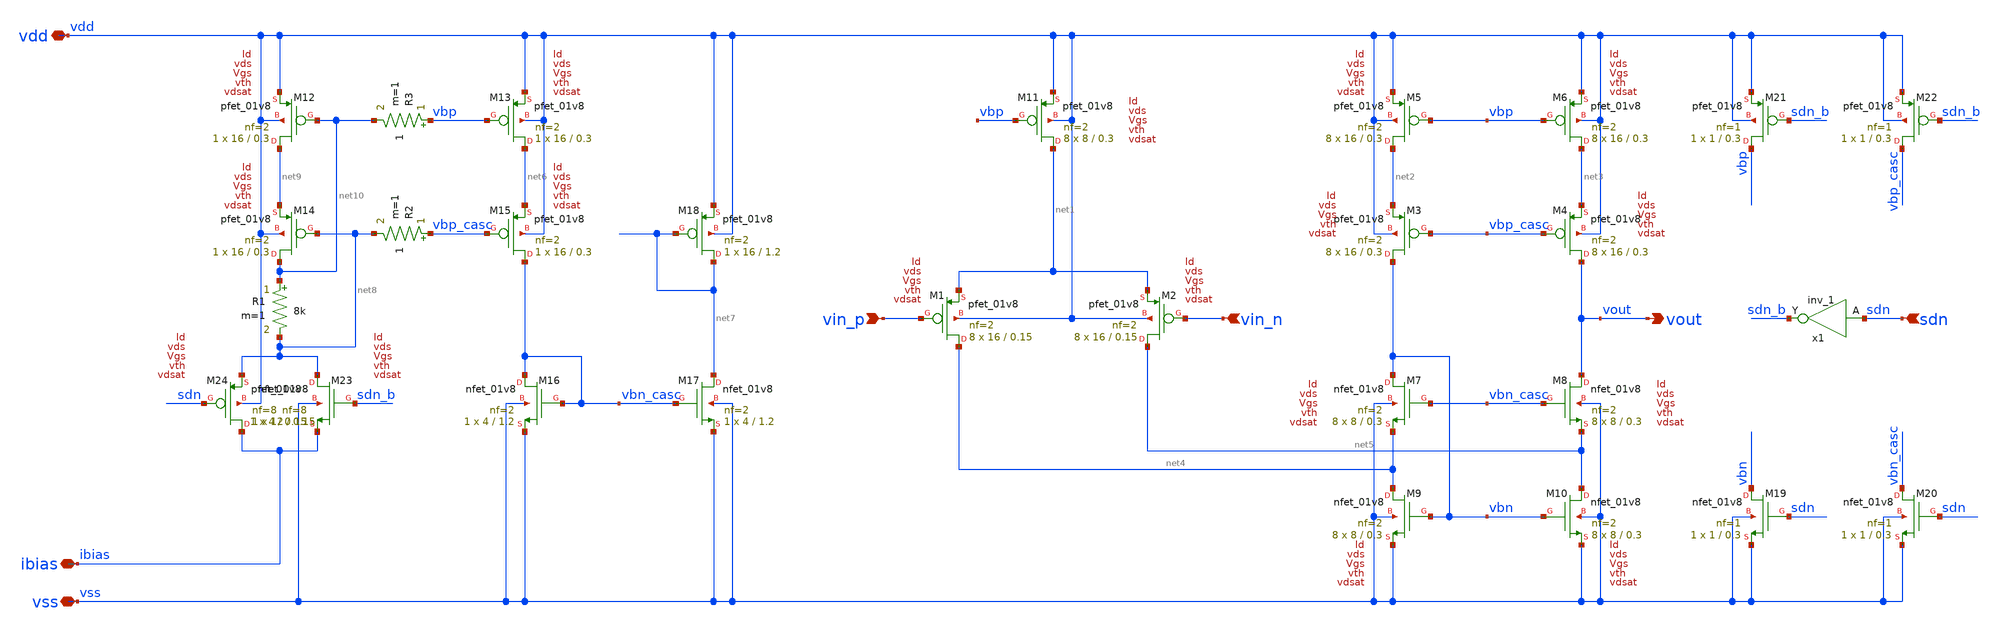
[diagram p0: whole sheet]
** sch_path: pll/pll_lf_buf/xschem/pll_lf_buf.sch
**.subckt pll_lf_buf vss vdd vin_p vin_n ibias vout sdn
*.iopin vss
*.iopin vdd
*.ipin vin_p
*.ipin vin_n
*.iopin ibias
*.opin vout
*.ipin sdn
XM1 net4 vin_p net1 vdd sky130_fd_pr__pfet_01v8 L=0.15 W=16 nf=2 ad='int((nf+1)/2) * W/nf * 0.29' as='int((nf+2)/2) * W/nf * 0.29'
+ pd='2*int((nf+1)/2) * (W/nf + 0.29)' ps='2*int((nf+2)/2) * (W/nf + 0.29)' nrd='0.29 / W' nrs='0.29 / W'
+ sa=0 sb=0 sd=0 mult=8 m=8
XM2 net5 vin_n net1 vdd sky130_fd_pr__pfet_01v8 L=0.15 W=16 nf=2 ad='int((nf+1)/2) * W/nf * 0.29' as='int((nf+2)/2) * W/nf * 0.29'
+ pd='2*int((nf+1)/2) * (W/nf + 0.29)' ps='2*int((nf+2)/2) * (W/nf + 0.29)' nrd='0.29 / W' nrs='0.29 / W'
+ sa=0 sb=0 sd=0 mult=8 m=8
XM3 vbn vbp_casc net2 vdd sky130_fd_pr__pfet_01v8 L=0.3 W=16 nf=2 ad='int((nf+1)/2) * W/nf * 0.29' as='int((nf+2)/2) * W/nf * 0.29'
+ pd='2*int((nf+1)/2) * (W/nf + 0.29)' ps='2*int((nf+2)/2) * (W/nf + 0.29)' nrd='0.29 / W' nrs='0.29 / W'
+ sa=0 sb=0 sd=0 mult=8 m=8
XM4 vout vbp_casc net3 vdd sky130_fd_pr__pfet_01v8 L=0.3 W=16 nf=2 ad='int((nf+1)/2) * W/nf * 0.29' as='int((nf+2)/2) * W/nf * 0.29'
+ pd='2*int((nf+1)/2) * (W/nf + 0.29)' ps='2*int((nf+2)/2) * (W/nf + 0.29)' nrd='0.29 / W' nrs='0.29 / W'
+ sa=0 sb=0 sd=0 mult=8 m=8
XM5 net2 vbp vdd vdd sky130_fd_pr__pfet_01v8 L=0.3 W=16 nf=2 ad='int((nf+1)/2) * W/nf * 0.29' as='int((nf+2)/2) * W/nf * 0.29'
+ pd='2*int((nf+1)/2) * (W/nf + 0.29)' ps='2*int((nf+2)/2) * (W/nf + 0.29)' nrd='0.29 / W' nrs='0.29 / W'
+ sa=0 sb=0 sd=0 mult=8 m=8
XM6 net3 vbp vdd vdd sky130_fd_pr__pfet_01v8 L=0.3 W=16 nf=2 ad='int((nf+1)/2) * W/nf * 0.29' as='int((nf+2)/2) * W/nf * 0.29'
+ pd='2*int((nf+1)/2) * (W/nf + 0.29)' ps='2*int((nf+2)/2) * (W/nf + 0.29)' nrd='0.29 / W' nrs='0.29 / W'
+ sa=0 sb=0 sd=0 mult=8 m=8
XM7 vbn vbn_casc net4 vss sky130_fd_pr__nfet_01v8 L=0.3 W=8 nf=2 ad='int((nf+1)/2) * W/nf * 0.29' as='int((nf+2)/2) * W/nf * 0.29'
+ pd='2*int((nf+1)/2) * (W/nf + 0.29)' ps='2*int((nf+2)/2) * (W/nf + 0.29)' nrd='0.29 / W' nrs='0.29 / W'
+ sa=0 sb=0 sd=0 mult=8 m=8
XM8 vout vbn_casc net5 vss sky130_fd_pr__nfet_01v8 L=0.3 W=8 nf=2 ad='int((nf+1)/2) * W/nf * 0.29' as='int((nf+2)/2) * W/nf * 0.29'
+ pd='2*int((nf+1)/2) * (W/nf + 0.29)' ps='2*int((nf+2)/2) * (W/nf + 0.29)' nrd='0.29 / W' nrs='0.29 / W'
+ sa=0 sb=0 sd=0 mult=8 m=8
XM9 net4 vbn vss vss sky130_fd_pr__nfet_01v8 L=0.3 W=8 nf=2 ad='int((nf+1)/2) * W/nf * 0.29' as='int((nf+2)/2) * W/nf * 0.29'
+ pd='2*int((nf+1)/2) * (W/nf + 0.29)' ps='2*int((nf+2)/2) * (W/nf + 0.29)' nrd='0.29 / W' nrs='0.29 / W'
+ sa=0 sb=0 sd=0 mult=8 m=8
XM10 net5 vbn vss vss sky130_fd_pr__nfet_01v8 L=0.3 W=8 nf=2 ad='int((nf+1)/2) * W/nf * 0.29' as='int((nf+2)/2) * W/nf * 0.29'
+ pd='2*int((nf+1)/2) * (W/nf + 0.29)' ps='2*int((nf+2)/2) * (W/nf + 0.29)' nrd='0.29 / W' nrs='0.29 / W'
+ sa=0 sb=0 sd=0 mult=8 m=8
XM11 net1 vbp vdd vdd sky130_fd_pr__pfet_01v8 L=0.3 W=8 nf=2 ad='int((nf+1)/2) * W/nf * 0.29' as='int((nf+2)/2) * W/nf * 0.29'
+ pd='2*int((nf+1)/2) * (W/nf + 0.29)' ps='2*int((nf+2)/2) * (W/nf + 0.29)' nrd='0.29 / W' nrs='0.29 / W'
+ sa=0 sb=0 sd=0 mult=8 m=8
XM12 net9 net10 vdd vdd sky130_fd_pr__pfet_01v8 L=0.3 W=16 nf=2 ad='int((nf+1)/2) * W/nf * 0.29' as='int((nf+2)/2) * W/nf * 0.29'
+ pd='2*int((nf+1)/2) * (W/nf + 0.29)' ps='2*int((nf+2)/2) * (W/nf + 0.29)' nrd='0.29 / W' nrs='0.29 / W'
+ sa=0 sb=0 sd=0 mult=1 m=1
XM13 net6 vbp vdd vdd sky130_fd_pr__pfet_01v8 L=0.3 W=16 nf=2 ad='int((nf+1)/2) * W/nf * 0.29' as='int((nf+2)/2) * W/nf * 0.29'
+ pd='2*int((nf+1)/2) * (W/nf + 0.29)' ps='2*int((nf+2)/2) * (W/nf + 0.29)' nrd='0.29 / W' nrs='0.29 / W'
+ sa=0 sb=0 sd=0 mult=1 m=1
XM14 net10 net8 net9 vdd sky130_fd_pr__pfet_01v8 L=0.3 W=16 nf=2 ad='int((nf+1)/2) * W/nf * 0.29' as='int((nf+2)/2) * W/nf * 0.29'
+ pd='2*int((nf+1)/2) * (W/nf + 0.29)' ps='2*int((nf+2)/2) * (W/nf + 0.29)' nrd='0.29 / W' nrs='0.29 / W'
+ sa=0 sb=0 sd=0 mult=1 m=1
XM15 vbn_casc vbp_casc net6 vdd sky130_fd_pr__pfet_01v8 L=0.3 W=16 nf=2 ad='int((nf+1)/2) * W/nf * 0.29'
+ as='int((nf+2)/2) * W/nf * 0.29' pd='2*int((nf+1)/2) * (W/nf + 0.29)' ps='2*int((nf+2)/2) * (W/nf + 0.29)'
+ nrd='0.29 / W' nrs='0.29 / W' sa=0 sb=0 sd=0 mult=1 m=1
XM16 vbn_casc vbn_casc vss vss sky130_fd_pr__nfet_01v8 L=1.2 W=4 nf=2 ad='int((nf+1)/2) * W/nf * 0.29'
+ as='int((nf+2)/2) * W/nf * 0.29' pd='2*int((nf+1)/2) * (W/nf + 0.29)' ps='2*int((nf+2)/2) * (W/nf + 0.29)'
+ nrd='0.29 / W' nrs='0.29 / W' sa=0 sb=0 sd=0 mult=1 m=1
XM17 net7 vbn_casc vss vss sky130_fd_pr__nfet_01v8 L=1.2 W=4 nf=2 ad='int((nf+1)/2) * W/nf * 0.29' as='int((nf+2)/2) * W/nf * 0.29'
+ pd='2*int((nf+1)/2) * (W/nf + 0.29)' ps='2*int((nf+2)/2) * (W/nf + 0.29)' nrd='0.29 / W' nrs='0.29 / W'
+ sa=0 sb=0 sd=0 mult=1 m=1
XM18 net7 net7 vdd vdd sky130_fd_pr__pfet_01v8 L=1.2 W=16 nf=2 ad='int((nf+1)/2) * W/nf * 0.29' as='int((nf+2)/2) * W/nf * 0.29'
+ pd='2*int((nf+1)/2) * (W/nf + 0.29)' ps='2*int((nf+2)/2) * (W/nf + 0.29)' nrd='0.29 / W' nrs='0.29 / W'
+ sa=0 sb=0 sd=0 mult=1 m=1
XM19 vbn sdn vss vss sky130_fd_pr__nfet_01v8 L=0.3 W=1 nf=1 ad='int((nf+1)/2) * W/nf * 0.29' as='int((nf+2)/2) * W/nf * 0.29'
+ pd='2*int((nf+1)/2) * (W/nf + 0.29)' ps='2*int((nf+2)/2) * (W/nf + 0.29)' nrd='0.29 / W' nrs='0.29 / W'
+ sa=0 sb=0 sd=0 mult=1 m=1
XM20 vbn_casc sdn vss vss sky130_fd_pr__nfet_01v8 L=0.3 W=1 nf=1 ad='int((nf+1)/2) * W/nf * 0.29' as='int((nf+2)/2) * W/nf * 0.29'
+ pd='2*int((nf+1)/2) * (W/nf + 0.29)' ps='2*int((nf+2)/2) * (W/nf + 0.29)' nrd='0.29 / W' nrs='0.29 / W'
+ sa=0 sb=0 sd=0 mult=1 m=1
XM21 vbp sdn_b vdd vdd sky130_fd_pr__pfet_01v8 L=0.3 W=1 nf=1 ad='int((nf+1)/2) * W/nf * 0.29' as='int((nf+2)/2) * W/nf * 0.29'
+ pd='2*int((nf+1)/2) * (W/nf + 0.29)' ps='2*int((nf+2)/2) * (W/nf + 0.29)' nrd='0.29 / W' nrs='0.29 / W'
+ sa=0 sb=0 sd=0 mult=1 m=1
XM22 vbp_casc sdn_b vdd vdd sky130_fd_pr__pfet_01v8 L=0.3 W=1 nf=1 ad='int((nf+1)/2) * W/nf * 0.29' as='int((nf+2)/2) * W/nf * 0.29'
+ pd='2*int((nf+1)/2) * (W/nf + 0.29)' ps='2*int((nf+2)/2) * (W/nf + 0.29)' nrd='0.29 / W' nrs='0.29 / W'
+ sa=0 sb=0 sd=0 mult=1 m=1
XM23 net8 sdn_b ibias vss sky130_fd_pr__nfet_01v8 L=0.15 W=4 nf=8 ad='int((nf+1)/2) * W/nf * 0.29' as='int((nf+2)/2) * W/nf * 0.29'
+ pd='2*int((nf+1)/2) * (W/nf + 0.29)' ps='2*int((nf+2)/2) * (W/nf + 0.29)' nrd='0.29 / W' nrs='0.29 / W'
+ sa=0 sb=0 sd=0 mult=1 m=1
x1 sdn vss vss vdd vdd sdn_b sky130_fd_sc_hd__inv_1
R1 net10 net8 8k m=1
R2 vbp_casc net8 1 m=1
R3 vbp net10 1 m=1
XM24 ibias sdn net8 vdd sky130_fd_pr__pfet_01v8 L=0.15 W=12 nf=8 ad='int((nf+1)/2) * W/nf * 0.29' as='int((nf+2)/2) * W/nf * 0.29'
+ pd='2*int((nf+1)/2) * (W/nf + 0.29)' ps='2*int((nf+2)/2) * (W/nf + 0.29)' nrd='0.29 / W' nrs='0.29 / W'
+ sa=0 sb=0 sd=0 mult=1 m=1
**** begin user architecture code

.options wnflag=1
.include $::SKYWATER_MODELS/cells/nfet_01v8/sky130_fd_pr__nfet_01v8__tt.corner.spice
.include $::SKYWATER_MODELS/cells/nfet_01v8_lvt/sky130_fd_pr__nfet_01v8_lvt__tt.corner.spice
.include $::SKYWATER_MODELS/cells/pfet_01v8/sky130_fd_pr__pfet_01v8__tt.corner.spice
.include $::SKYWATER_MODELS/cells/nfet_03v3_nvt/sky130_fd_pr__nfet_03v3_nvt__tt.corner.spice
.include $::SKYWATER_MODELS/cells/nfet_05v0_nvt/sky130_fd_pr__nfet_05v0_nvt__tt.corner.spice
.include $::SKYWATER_MODELS/cells/esd_nfet_01v8/sky130_fd_pr__esd_nfet_01v8__tt.corner.spice
.include $::SKYWATER_MODELS/cells/pfet_01v8_lvt/sky130_fd_pr__pfet_01v8_lvt__tt.corner.spice
.include $::SKYWATER_MODELS/cells/pfet_01v8_hvt/sky130_fd_pr__pfet_01v8_hvt__tt.corner.spice
.include $::SKYWATER_MODELS/cells/esd_pfet_g5v0d10v5/sky130_fd_pr__esd_pfet_g5v0d10v5__tt.corner.spice
.include $::SKYWATER_MODELS/cells/pfet_g5v0d10v5/sky130_fd_pr__pfet_g5v0d10v5__tt.corner.spice
.include $::SKYWATER_MODELS/cells/pfet_g5v0d16v0/sky130_fd_pr__pfet_g5v0d16v0__tt.corner.spice
.include $::SKYWATER_MODELS/cells/nfet_g5v0d10v5/sky130_fd_pr__nfet_g5v0d10v5__tt.corner.spice
.include $::SKYWATER_MODELS/cells/nfet_g5v0d16v0/sky130_fd_pr__nfet_g5v0d16v0__tt_discrete.corner.spice
.include $::SKYWATER_MODELS/cells/esd_nfet_g5v0d10v5/sky130_fd_pr__esd_nfet_g5v0d10v5__tt.corner.spice
.include $::SKYWATER_MODELS/models/corners/tt/nonfet.spice

.include $::SKYWATER_MODELS/cells/cap_var_hvt/sky130_fd_pr__cap_var_hvt.model.spice

* Mismatch parameters
.include $::SKYWATER_MODELS/cells/nfet_01v8/sky130_fd_pr__nfet_01v8__mismatch.corner.spice
.include $::SKYWATER_MODELS/cells/pfet_01v8/sky130_fd_pr__pfet_01v8__mismatch.corner.spice
.include $::SKYWATER_MODELS/cells/nfet_01v8_lvt/sky130_fd_pr__nfet_01v8_lvt__mismatch.corner.spice
.include $::SKYWATER_MODELS/cells/pfet_01v8_lvt/sky130_fd_pr__pfet_01v8_lvt__mismatch.corner.spice
.include $::SKYWATER_MODELS/cells/pfet_01v8_hvt/sky130_fd_pr__pfet_01v8_hvt__mismatch.corner.spice
.include $::SKYWATER_MODELS/cells/nfet_g5v0d10v5/sky130_fd_pr__nfet_g5v0d10v5__mismatch.corner.spice
.include $::SKYWATER_MODELS/cells/pfet_g5v0d10v5/sky130_fd_pr__pfet_g5v0d10v5__mismatch.corner.spice
.include $::SKYWATER_MODELS/cells/nfet_05v0_nvt/sky130_fd_pr__nfet_05v0_nvt__mismatch.corner.spice
.include $::SKYWATER_MODELS/cells/nfet_03v3_nvt/sky130_fd_pr__nfet_03v3_nvt__mismatch.corner.spice

* Resistor$::SKYWATER_MODELS/Capacitor
.include $::SKYWATER_MODELS/models/r+c/res_typical__cap_typical.spice
.include $::SKYWATER_MODELS/models/r+c/res_typical__cap_typical__lin.spice

* Special cells
.include $::SKYWATER_MODELS/models/corners/tt/specialized_cells.spice

* All models
.include $::SKYWATER_MODELS/models/all.spice

* Corner
.include $::SKYWATER_MODELS/models/corners/tt/rf.spice


.include $::SKYWATER_STDCELLS/cells/inv/sky130_fd_sc_hd__inv_1.spice
.include $::SKYWATER_STDCELLS/cells/inv/sky130_fd_sc_hd__inv_2.spice
.include $::SKYWATER_STDCELLS/cells/inv/sky130_fd_sc_hd__inv_4.spice
.include $::SKYWATER_STDCELLS/cells/inv/sky130_fd_sc_hd__inv_8.spice

**** end user architecture code
**.ends
.end
